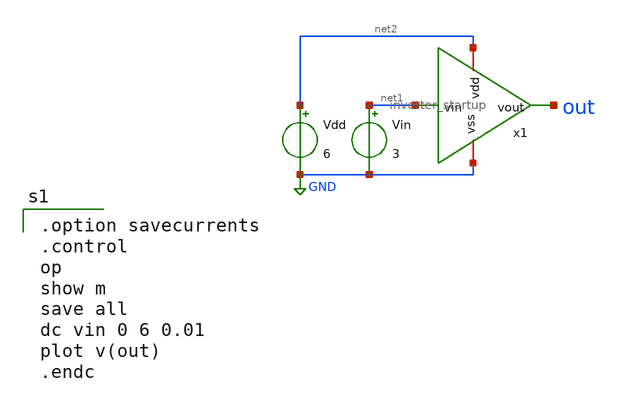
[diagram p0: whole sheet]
** sch_path: member_project/DCDC/ShuntaroOHNO/xschem/inverter_startup_dc.sch
**.subckt inverter_startup_dc
Vdd net2 GND 6
Vin net1 GND 3
x1 net2 net1 out GND inverter_startup
**** begin user architecture code
 .include $::LIB/ip62_models

.option savecurrents
.control
op
show m
save all
dc vin 0 6 0.01
plot v(out)
.endc

**** end user architecture code
**.ends

* expanding   symbol:  inverter_startup.sym # of pins=4
** sym_path: member_project/DCDC/ShuntaroOHNO/xschem/inverter_startup.sym
** sch_path: member_project/DCDC/ShuntaroOHNO/xschem/inverter_startup.sch
.subckt inverter_startup vdd vin vout vss
*.iopin vdd
*.iopin vss
*.ipin vin
*.opin vout
XM1 vout vin vdd vdd PMOS w=3.4u l=30u as=0 ad=0 ps=0 pd=0 nrd=0 nrs=0 m=1
XM2 vout vin vss vss NMOS w=30u l=3.4u as=0 ad=0 ps=0 pd=0 nrd=0 nrs=0 m=1
.ends

.GLOBAL GND
.end
